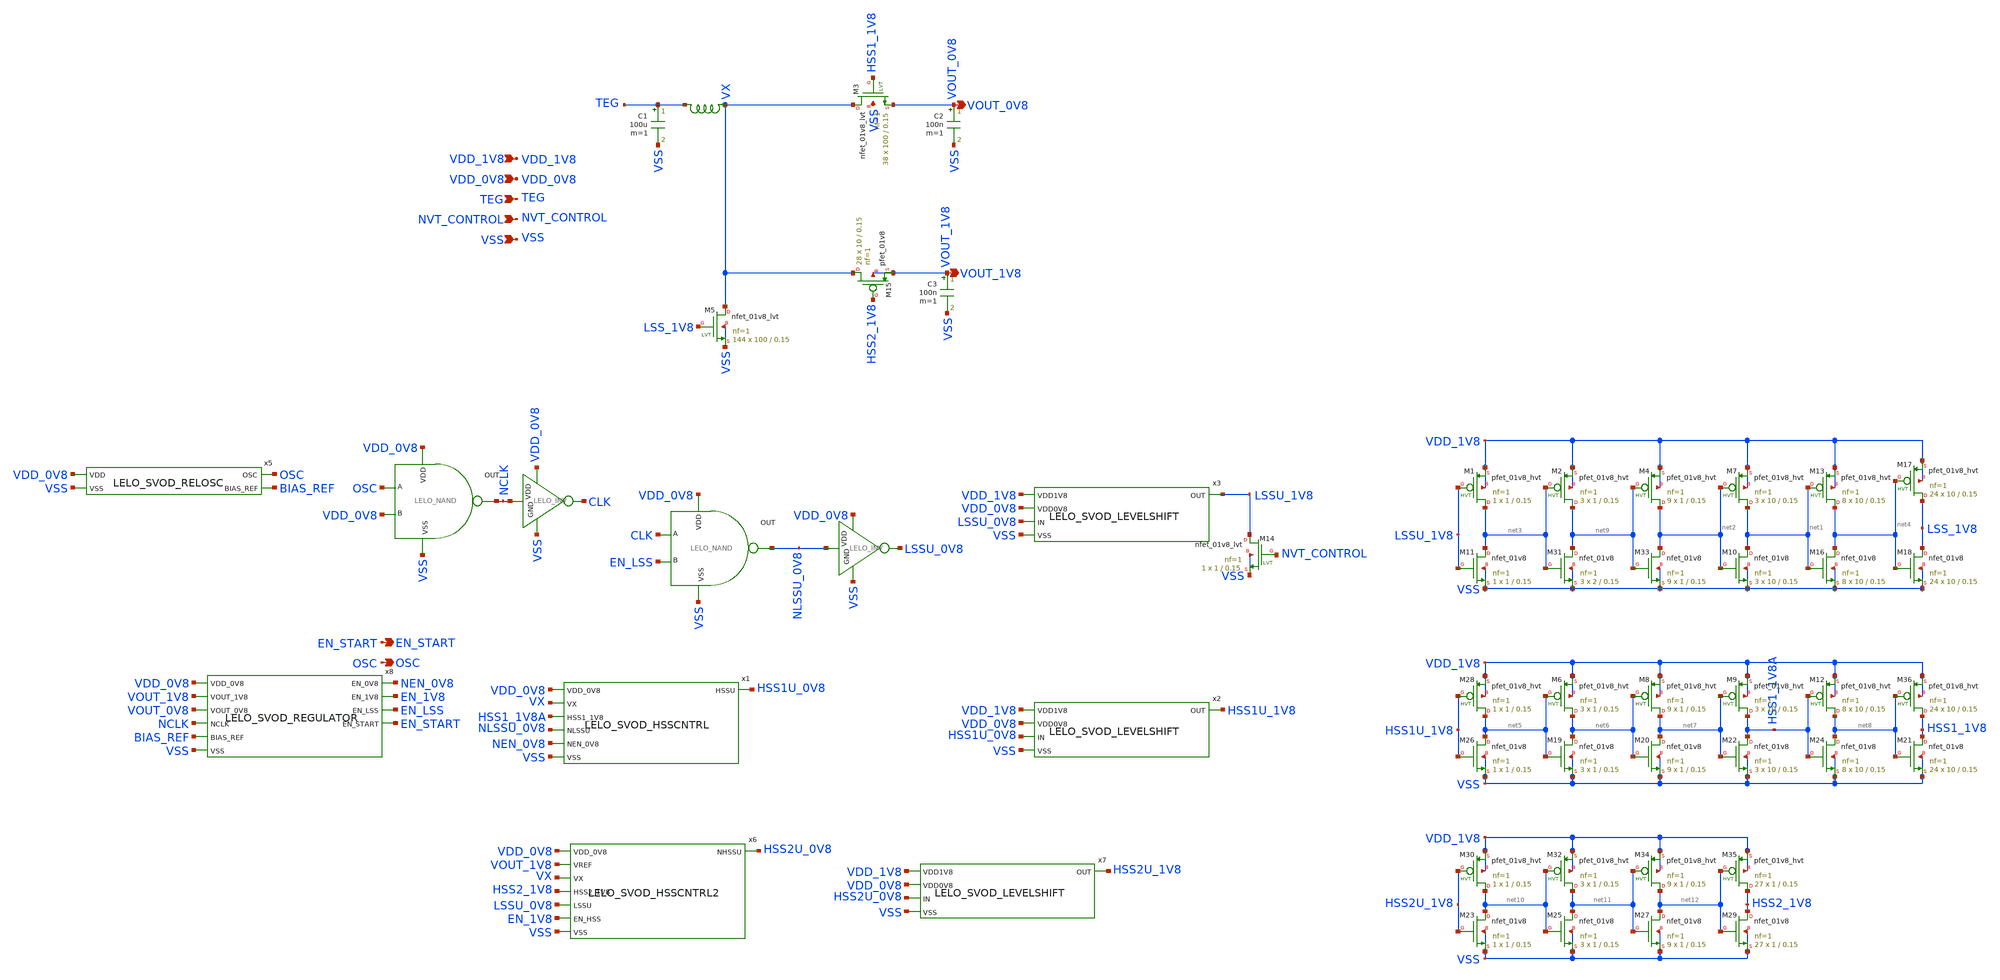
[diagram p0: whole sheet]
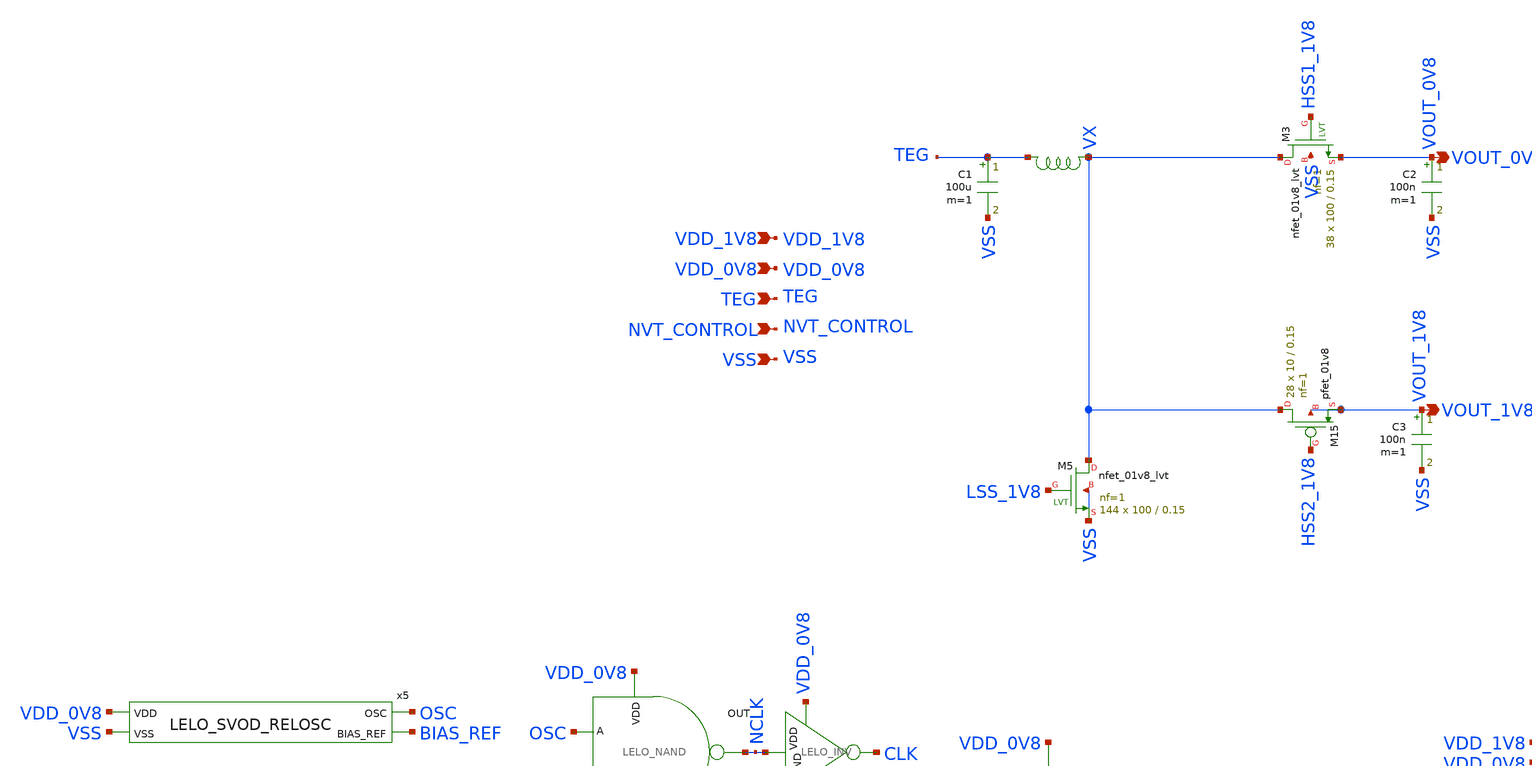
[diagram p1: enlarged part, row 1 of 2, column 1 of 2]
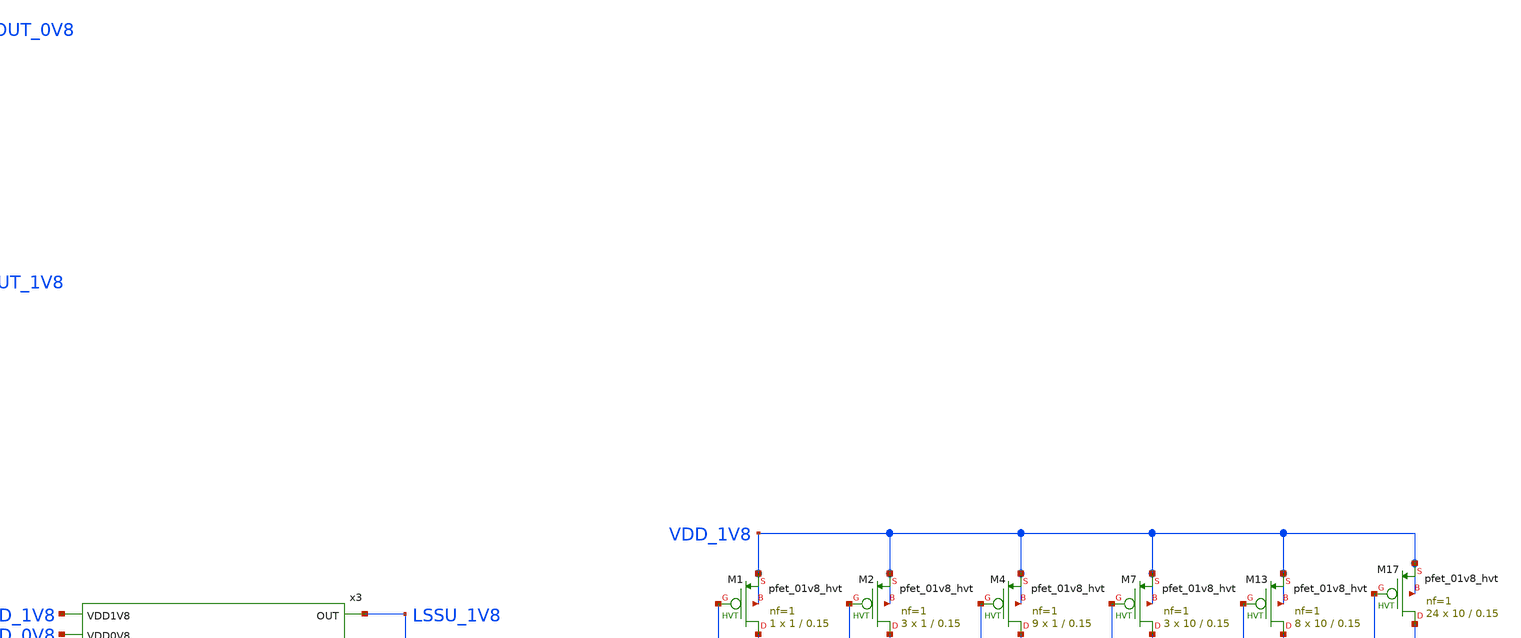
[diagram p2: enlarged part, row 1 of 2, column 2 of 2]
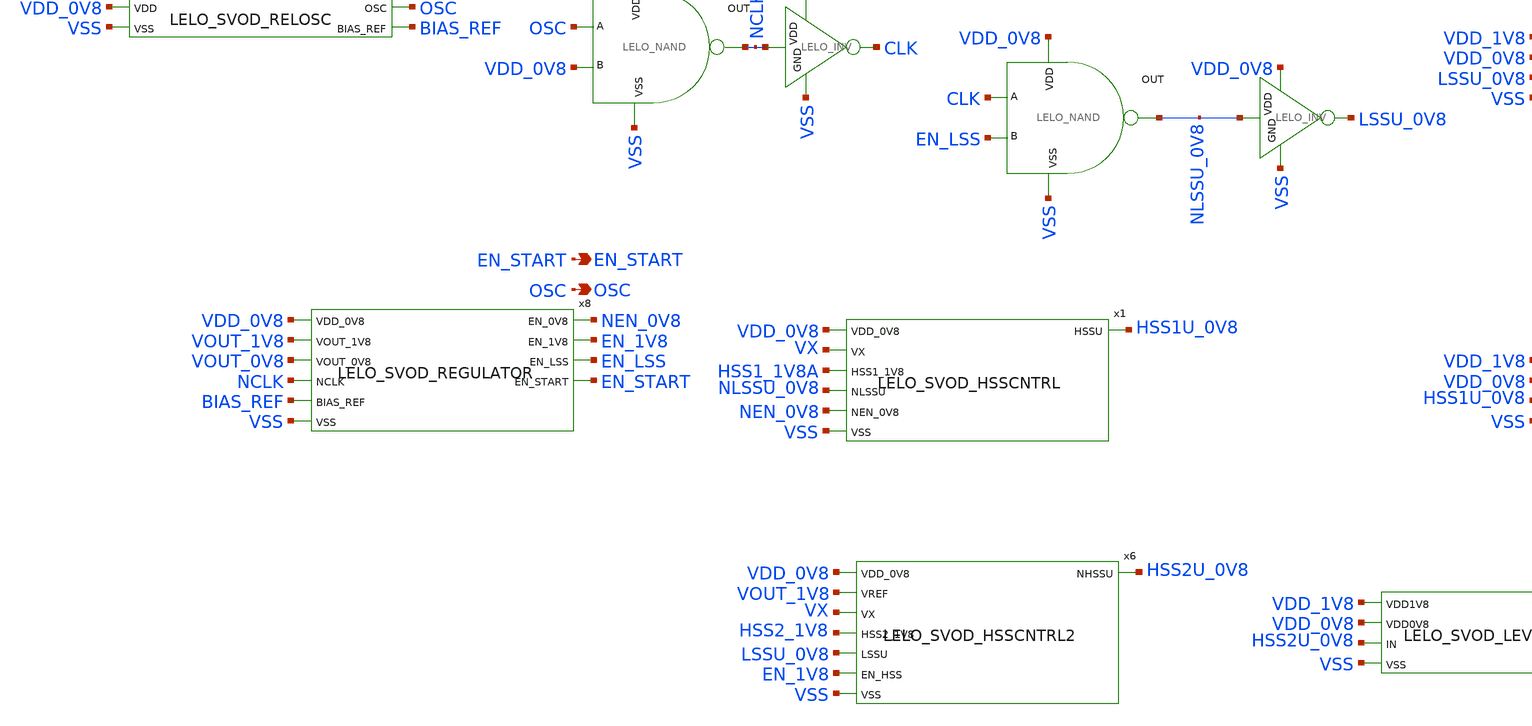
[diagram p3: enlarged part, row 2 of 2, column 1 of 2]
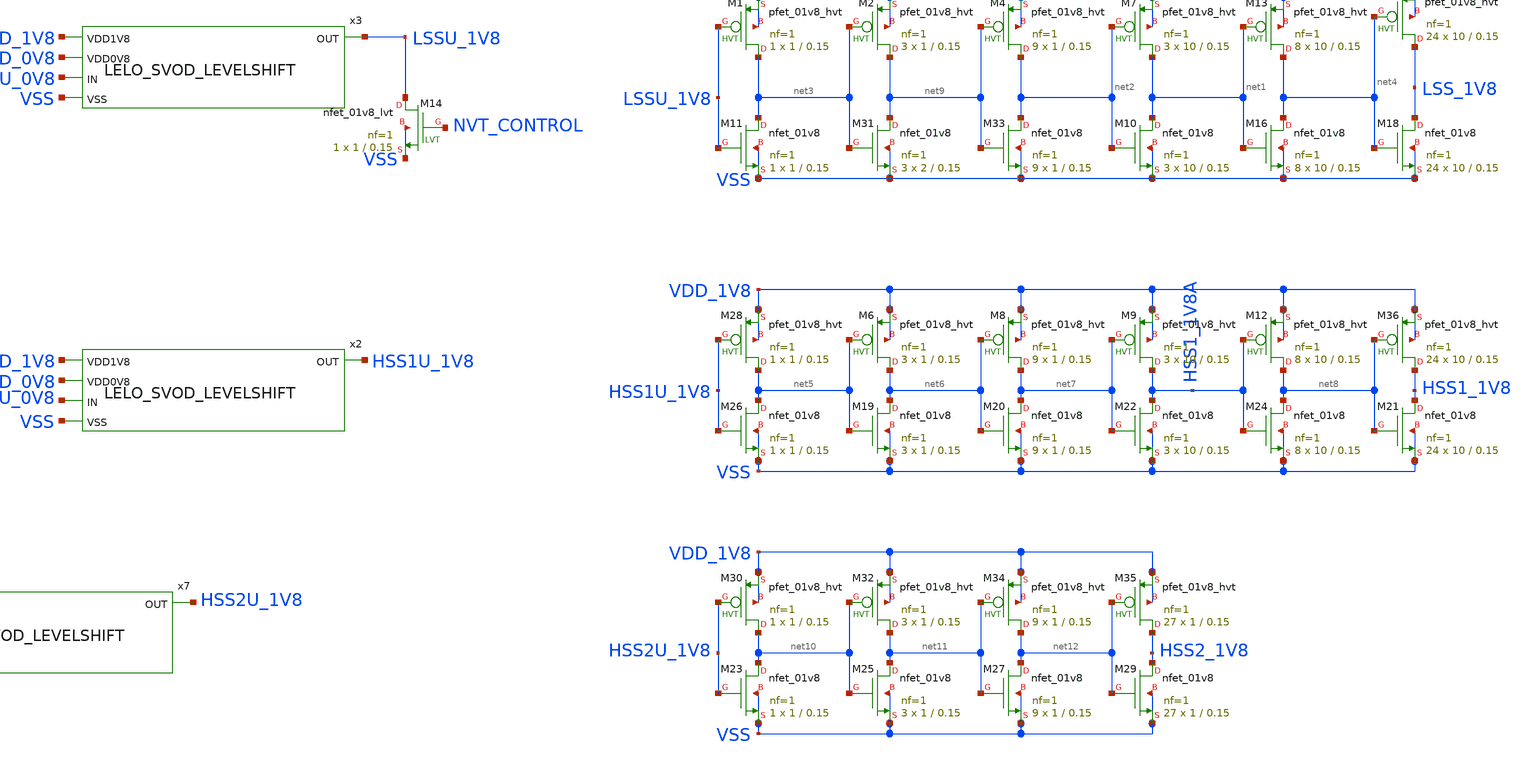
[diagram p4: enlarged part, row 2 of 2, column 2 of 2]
** sch_path: design/LELO_SVOD_SKY130A/LELO_SVOD_BOOST_2.sch
**.subckt LELO_SVOD_BOOST_2 VSS TEG VDD_0V8 VDD_1V8 VOUT_0V8 VOUT_1V8 EN_START OSC NVT_CONTROL
*.ipin VSS
*.ipin TEG
*.ipin VDD_0V8
*.ipin VDD_1V8
*.opin VOUT_0V8
*.opin VOUT_1V8
*.opin EN_START
*.opin OSC
*.ipin NVT_CONTROL
C1 TEG VSS 100u m=1
XM5 VX LSS_1V8 VSS VSS sky130_fd_pr__nfet_01v8_lvt L=0.15 W=100 nf=1 ad='int((1 + 1)/2) * 100 / 1 * 0.29'
+ as='int((1 + 2)/2) * 100 / 1 * 0.29' pd='2*int((1 + 1)/2) * (100 / 1 + 0.29)' ps='2*int((1 + 2)/2) * (100 / 1 + 0.29)'
+ nrd='0.29 / 100 ' nrs='0.29 / 100 ' sa=0 sb=0 sd=0 mult=144 m=144
C2 VOUT_0V8 VSS 100n m=1
XM11 net3 LSSU_1V8 VSS VSS sky130_fd_pr__nfet_01v8 L=0.15 W=1 nf=1 ad='int((1 + 1)/2) * 1 / 1 * 0.29'
+ as='int((1 + 2)/2) * 1 / 1 * 0.29' pd='2*int((1 + 1)/2) * (1 / 1 + 0.29)' ps='2*int((1 + 2)/2) * (1 / 1 + 0.29)'
+ nrd='0.29 / 1 ' nrs='0.29 / 1 ' sa=0 sb=0 sd=0 mult=1 m=1
XM24 net8 HSS1_1V8A VSS VSS sky130_fd_pr__nfet_01v8 L=0.15 W=10 nf=1 ad='int((1 + 1)/2) * 10 / 1 * 0.29'
+ as='int((1 + 2)/2) * 10 / 1 * 0.29' pd='2*int((1 + 1)/2) * (10 / 1 + 0.29)' ps='2*int((1 + 2)/2) * (10 / 1 + 0.29)'
+ nrd='0.29 / 10 ' nrs='0.29 / 10 ' sa=0 sb=0 sd=0 mult=8 m=8
XM31 net9 net3 VSS VSS sky130_fd_pr__nfet_01v8 L=0.15 W=2 nf=1 ad='int((1 + 1)/2) * 2 / 1 * 0.29' as='int((1 + 2)/2) * 2 / 1 * 0.29'
+ pd='2*int((1 + 1)/2) * (2 / 1 + 0.29)' ps='2*int((1 + 2)/2) * (2 / 1 + 0.29)' nrd='0.29 / 2 ' nrs='0.29 / 2 '
+ sa=0 sb=0 sd=0 mult=3 m=3
XM33 net2 net9 VSS VSS sky130_fd_pr__nfet_01v8 L=0.15 W=1 nf=1 ad='int((1 + 1)/2) * 1 / 1 * 0.29' as='int((1 + 2)/2) * 1 / 1 * 0.29'
+ pd='2*int((1 + 1)/2) * (1 / 1 + 0.29)' ps='2*int((1 + 2)/2) * (1 / 1 + 0.29)' nrd='0.29 / 1 ' nrs='0.29 / 1 '
+ sa=0 sb=0 sd=0 mult=9 m=9
XM3 VX HSS1_1V8 VOUT_0V8 VSS sky130_fd_pr__nfet_01v8_lvt L=0.15 W=100 nf=1 ad='int((1 + 1)/2) * 100 / 1 * 0.29'
+ as='int((1 + 2)/2) * 100 / 1 * 0.29' pd='2*int((1 + 1)/2) * (100 / 1 + 0.29)' ps='2*int((1 + 2)/2) * (100 / 1 + 0.29)'
+ nrd='0.29 / 100 ' nrs='0.29 / 100 ' sa=0 sb=0 sd=0 mult=38 m=38
x1 VDD_0V8 VX HSS1_1V8A NLSSU_0V8 HSS1U_0V8 NEN_0V8 VSS LELO_SVOD_HSSCNTRL
x2 VDD_1V8 HSS1U_1V8 VDD_0V8 HSS1U_0V8 VSS LELO_SVOD_LEVELSHIFT
x3 VDD_1V8 LSSU_1V8 VDD_0V8 LSSU_0V8 VSS LELO_SVOD_LEVELSHIFT
XM12 net8 HSS1_1V8A VDD_1V8 VDD_1V8 sky130_fd_pr__pfet_01v8_hvt L=0.15 W=10 nf=1 ad='int((1 + 1)/2) * 10 / 1 * 0.29'
+ as='int((1 + 2)/2) * 10 / 1 * 0.29' pd='2*int((1 + 1)/2) * (10 / 1 + 0.29)' ps='2*int((1 + 2)/2) * (10 / 1 + 0.29)'
+ nrd='0.29 / 10 ' nrs='0.29 / 10 ' sa=0 sb=0 sd=0 mult=8 m=8
XM1 net3 LSSU_1V8 VDD_1V8 VDD_1V8 sky130_fd_pr__pfet_01v8_hvt L=0.15 W=1 nf=1 ad='int((1 + 1)/2) * 1 / 1 * 0.29'
+ as='int((1 + 2)/2) * 1 / 1 * 0.29' pd='2*int((1 + 1)/2) * (1 / 1 + 0.29)' ps='2*int((1 + 2)/2) * (1 / 1 + 0.29)'
+ nrd='0.29 / 1 ' nrs='0.29 / 1 ' sa=0 sb=0 sd=0 mult=1 m=1
XM2 net9 net3 VDD_1V8 VDD_1V8 sky130_fd_pr__pfet_01v8_hvt L=0.15 W=1 nf=1 ad='int((1 + 1)/2) * 1 / 1 * 0.29'
+ as='int((1 + 2)/2) * 1 / 1 * 0.29' pd='2*int((1 + 1)/2) * (1 / 1 + 0.29)' ps='2*int((1 + 2)/2) * (1 / 1 + 0.29)'
+ nrd='0.29 / 1 ' nrs='0.29 / 1 ' sa=0 sb=0 sd=0 mult=3 m=3
XM4 net2 net9 VDD_1V8 VDD_1V8 sky130_fd_pr__pfet_01v8_hvt L=0.15 W=1 nf=1 ad='int((1 + 1)/2) * 1 / 1 * 0.29'
+ as='int((1 + 2)/2) * 1 / 1 * 0.29' pd='2*int((1 + 1)/2) * (1 / 1 + 0.29)' ps='2*int((1 + 2)/2) * (1 / 1 + 0.29)'
+ nrd='0.29 / 1 ' nrs='0.29 / 1 ' sa=0 sb=0 sd=0 mult=9 m=9
x4 VX TEG XGL6030-183_sat
x5 VDD_0V8 OSC BIAS_REF VSS LELO_SVOD_RELOSC
XM15 VX HSS2_1V8 VOUT_1V8 VOUT_1V8 sky130_fd_pr__pfet_01v8 L=0.15 W=10 nf=1 ad='int((1 + 1)/2) * 10 / 1 * 0.29'
+ as='int((1 + 2)/2) * 10 / 1 * 0.29' pd='2*int((1 + 1)/2) * (10 / 1 + 0.29)' ps='2*int((1 + 2)/2) * (10 / 1 + 0.29)'
+ nrd='0.29 / 10 ' nrs='0.29 / 10 ' sa=0 sb=0 sd=0 mult=28 m=28
C3 VOUT_1V8 VSS 100n m=1
x6 VDD_0V8 HSS2U_0V8 VOUT_1V8 VX HSS2_1V8 LSSU_0V8 EN_1V8 VSS LELO_SVOD_HSSCNTRL2
x7 VDD_1V8 HSS2U_1V8 VDD_0V8 HSS2U_0V8 VSS LELO_SVOD_LEVELSHIFT
XM23 net10 HSS2U_1V8 VSS VSS sky130_fd_pr__nfet_01v8 L=0.15 W=1 nf=1 ad='int((1 + 1)/2) * 1 / 1 * 0.29'
+ as='int((1 + 2)/2) * 1 / 1 * 0.29' pd='2*int((1 + 1)/2) * (1 / 1 + 0.29)' ps='2*int((1 + 2)/2) * (1 / 1 + 0.29)'
+ nrd='0.29 / 1 ' nrs='0.29 / 1 ' sa=0 sb=0 sd=0 mult=1 m=1
XM25 net11 net10 VSS VSS sky130_fd_pr__nfet_01v8 L=0.15 W=1 nf=1 ad='int((1 + 1)/2) * 1 / 1 * 0.29' as='int((1 + 2)/2) * 1 / 1 * 0.29'
+ pd='2*int((1 + 1)/2) * (1 / 1 + 0.29)' ps='2*int((1 + 2)/2) * (1 / 1 + 0.29)' nrd='0.29 / 1 ' nrs='0.29 / 1 '
+ sa=0 sb=0 sd=0 mult=3 m=3
XM27 net12 net11 VSS VSS sky130_fd_pr__nfet_01v8 L=0.15 W=1 nf=1 ad='int((1 + 1)/2) * 1 / 1 * 0.29' as='int((1 + 2)/2) * 1 / 1 * 0.29'
+ pd='2*int((1 + 1)/2) * (1 / 1 + 0.29)' ps='2*int((1 + 2)/2) * (1 / 1 + 0.29)' nrd='0.29 / 1 ' nrs='0.29 / 1 '
+ sa=0 sb=0 sd=0 mult=9 m=9
XM29 HSS2_1V8 net12 VSS VSS sky130_fd_pr__nfet_01v8 L=0.15 W=1 nf=1 ad='int((1 + 1)/2) * 1 / 1 * 0.29'
+ as='int((1 + 2)/2) * 1 / 1 * 0.29' pd='2*int((1 + 1)/2) * (1 / 1 + 0.29)' ps='2*int((1 + 2)/2) * (1 / 1 + 0.29)'
+ nrd='0.29 / 1 ' nrs='0.29 / 1 ' sa=0 sb=0 sd=0 mult=27 m=27
XM30 net10 HSS2U_1V8 VDD_1V8 VDD_1V8 sky130_fd_pr__pfet_01v8_hvt L=0.15 W=1 nf=1 ad='int((1 + 1)/2) * 1 / 1 * 0.29'
+ as='int((1 + 2)/2) * 1 / 1 * 0.29' pd='2*int((1 + 1)/2) * (1 / 1 + 0.29)' ps='2*int((1 + 2)/2) * (1 / 1 + 0.29)'
+ nrd='0.29 / 1 ' nrs='0.29 / 1 ' sa=0 sb=0 sd=0 mult=1 m=1
XM32 net11 net10 VDD_1V8 VDD_1V8 sky130_fd_pr__pfet_01v8_hvt L=0.15 W=1 nf=1 ad='int((1 + 1)/2) * 1 / 1 * 0.29'
+ as='int((1 + 2)/2) * 1 / 1 * 0.29' pd='2*int((1 + 1)/2) * (1 / 1 + 0.29)' ps='2*int((1 + 2)/2) * (1 / 1 + 0.29)'
+ nrd='0.29 / 1 ' nrs='0.29 / 1 ' sa=0 sb=0 sd=0 mult=3 m=3
XM34 net12 net11 VDD_1V8 VDD_1V8 sky130_fd_pr__pfet_01v8_hvt L=0.15 W=1 nf=1 ad='int((1 + 1)/2) * 1 / 1 * 0.29'
+ as='int((1 + 2)/2) * 1 / 1 * 0.29' pd='2*int((1 + 1)/2) * (1 / 1 + 0.29)' ps='2*int((1 + 2)/2) * (1 / 1 + 0.29)'
+ nrd='0.29 / 1 ' nrs='0.29 / 1 ' sa=0 sb=0 sd=0 mult=9 m=9
XM35 HSS2_1V8 net12 VDD_1V8 VDD_1V8 sky130_fd_pr__pfet_01v8_hvt L=0.15 W=1 nf=1 ad='int((1 + 1)/2) * 1 / 1 * 0.29'
+ as='int((1 + 2)/2) * 1 / 1 * 0.29' pd='2*int((1 + 1)/2) * (1 / 1 + 0.29)' ps='2*int((1 + 2)/2) * (1 / 1 + 0.29)'
+ nrd='0.29 / 1 ' nrs='0.29 / 1 ' sa=0 sb=0 sd=0 mult=27 m=27
x8 NEN_0V8 EN_1V8 EN_LSS VDD_0V8 EN_START VOUT_1V8 VOUT_0V8 NCLK BIAS_REF VSS LELO_SVOD_REGULATOR
x9 VDD_0V8 NLSSU_0V8 CLK EN_LSS VSS LELO_NAND
x10 VDD_0V8 NLSSU_0V8 LSSU_0V8 VSS LELO_INV
x11 VDD_0V8 NCLK CLK VSS LELO_INV
x13 VDD_0V8 NCLK OSC VDD_0V8 VSS LELO_NAND
XM14 LSSU_1V8 NVT_CONTROL VSS VSS sky130_fd_pr__nfet_01v8_lvt L=0.15 W=1 nf=1 ad='int((1 + 1)/2) * 1 / 1 * 0.29'
+ as='int((1 + 2)/2) * 1 / 1 * 0.29' pd='2*int((1 + 1)/2) * (1 / 1 + 0.29)' ps='2*int((1 + 2)/2) * (1 / 1 + 0.29)'
+ nrd='0.29 / 1 ' nrs='0.29 / 1 ' sa=0 sb=0 sd=0 mult=1 m=1
XM26 net5 HSS1U_1V8 VSS VSS sky130_fd_pr__nfet_01v8 L=0.15 W=1 nf=1 ad='int((1 + 1)/2) * 1 / 1 * 0.29'
+ as='int((1 + 2)/2) * 1 / 1 * 0.29' pd='2*int((1 + 1)/2) * (1 / 1 + 0.29)' ps='2*int((1 + 2)/2) * (1 / 1 + 0.29)'
+ nrd='0.29 / 1 ' nrs='0.29 / 1 ' sa=0 sb=0 sd=0 mult=1 m=1
XM28 net5 HSS1U_1V8 VDD_1V8 VDD_1V8 sky130_fd_pr__pfet_01v8_hvt L=0.15 W=1 nf=1 ad='int((1 + 1)/2) * 1 / 1 * 0.29'
+ as='int((1 + 2)/2) * 1 / 1 * 0.29' pd='2*int((1 + 1)/2) * (1 / 1 + 0.29)' ps='2*int((1 + 2)/2) * (1 / 1 + 0.29)'
+ nrd='0.29 / 1 ' nrs='0.29 / 1 ' sa=0 sb=0 sd=0 mult=1 m=1
XM21 HSS1_1V8 net8 VSS VSS sky130_fd_pr__nfet_01v8 L=0.15 W=10 nf=1 ad='int((1 + 1)/2) * 10 / 1 * 0.29'
+ as='int((1 + 2)/2) * 10 / 1 * 0.29' pd='2*int((1 + 1)/2) * (10 / 1 + 0.29)' ps='2*int((1 + 2)/2) * (10 / 1 + 0.29)'
+ nrd='0.29 / 10 ' nrs='0.29 / 10 ' sa=0 sb=0 sd=0 mult=24 m=24
XM36 HSS1_1V8 net8 VDD_1V8 VDD_1V8 sky130_fd_pr__pfet_01v8_hvt L=0.15 W=10 nf=1 ad='int((1 + 1)/2) * 10 / 1 * 0.29'
+ as='int((1 + 2)/2) * 10 / 1 * 0.29' pd='2*int((1 + 1)/2) * (10 / 1 + 0.29)' ps='2*int((1 + 2)/2) * (10 / 1 + 0.29)'
+ nrd='0.29 / 10 ' nrs='0.29 / 10 ' sa=0 sb=0 sd=0 mult=24 m=24
XM6 net6 net5 VDD_1V8 VDD_1V8 sky130_fd_pr__pfet_01v8_hvt L=0.15 W=1 nf=1 ad='int((1 + 1)/2) * 1 / 1 * 0.29'
+ as='int((1 + 2)/2) * 1 / 1 * 0.29' pd='2*int((1 + 1)/2) * (1 / 1 + 0.29)' ps='2*int((1 + 2)/2) * (1 / 1 + 0.29)'
+ nrd='0.29 / 1 ' nrs='0.29 / 1 ' sa=0 sb=0 sd=0 mult=3 m=3
XM19 net6 net5 VSS VSS sky130_fd_pr__nfet_01v8 L=0.15 W=1 nf=1 ad='int((1 + 1)/2) * 1 / 1 * 0.29' as='int((1 + 2)/2) * 1 / 1 * 0.29'
+ pd='2*int((1 + 1)/2) * (1 / 1 + 0.29)' ps='2*int((1 + 2)/2) * (1 / 1 + 0.29)' nrd='0.29 / 1 ' nrs='0.29 / 1 '
+ sa=0 sb=0 sd=0 mult=3 m=3
XM8 net7 net6 VDD_1V8 VDD_1V8 sky130_fd_pr__pfet_01v8_hvt L=0.15 W=1 nf=1 ad='int((1 + 1)/2) * 1 / 1 * 0.29'
+ as='int((1 + 2)/2) * 1 / 1 * 0.29' pd='2*int((1 + 1)/2) * (1 / 1 + 0.29)' ps='2*int((1 + 2)/2) * (1 / 1 + 0.29)'
+ nrd='0.29 / 1 ' nrs='0.29 / 1 ' sa=0 sb=0 sd=0 mult=9 m=9
XM20 net7 net6 VSS VSS sky130_fd_pr__nfet_01v8 L=0.15 W=1 nf=1 ad='int((1 + 1)/2) * 1 / 1 * 0.29' as='int((1 + 2)/2) * 1 / 1 * 0.29'
+ pd='2*int((1 + 1)/2) * (1 / 1 + 0.29)' ps='2*int((1 + 2)/2) * (1 / 1 + 0.29)' nrd='0.29 / 1 ' nrs='0.29 / 1 '
+ sa=0 sb=0 sd=0 mult=9 m=9
XM9 HSS1_1V8A net7 VDD_1V8 VDD_1V8 sky130_fd_pr__pfet_01v8_hvt L=0.15 W=10 nf=1 ad='int((1 + 1)/2) * 10 / 1 * 0.29'
+ as='int((1 + 2)/2) * 10 / 1 * 0.29' pd='2*int((1 + 1)/2) * (10 / 1 + 0.29)' ps='2*int((1 + 2)/2) * (10 / 1 + 0.29)'
+ nrd='0.29 / 10 ' nrs='0.29 / 10 ' sa=0 sb=0 sd=0 mult=3 m=3
XM22 HSS1_1V8A net7 VSS VSS sky130_fd_pr__nfet_01v8 L=0.15 W=10 nf=1 ad='int((1 + 1)/2) * 10 / 1 * 0.29'
+ as='int((1 + 2)/2) * 10 / 1 * 0.29' pd='2*int((1 + 1)/2) * (10 / 1 + 0.29)' ps='2*int((1 + 2)/2) * (10 / 1 + 0.29)'
+ nrd='0.29 / 10 ' nrs='0.29 / 10 ' sa=0 sb=0 sd=0 mult=3 m=3
XM7 net1 net2 VDD_1V8 VDD_1V8 sky130_fd_pr__pfet_01v8_hvt L=0.15 W=10 nf=1 ad='int((1 + 1)/2) * 10 / 1 * 0.29'
+ as='int((1 + 2)/2) * 10 / 1 * 0.29' pd='2*int((1 + 1)/2) * (10 / 1 + 0.29)' ps='2*int((1 + 2)/2) * (10 / 1 + 0.29)'
+ nrd='0.29 / 10 ' nrs='0.29 / 10 ' sa=0 sb=0 sd=0 mult=3 m=3
XM10 net1 net2 VSS VSS sky130_fd_pr__nfet_01v8 L=0.15 W=10 nf=1 ad='int((1 + 1)/2) * 10 / 1 * 0.29' as='int((1 + 2)/2) * 10 / 1 * 0.29'
+ pd='2*int((1 + 1)/2) * (10 / 1 + 0.29)' ps='2*int((1 + 2)/2) * (10 / 1 + 0.29)' nrd='0.29 / 10 ' nrs='0.29 / 10 '
+ sa=0 sb=0 sd=0 mult=3 m=3
XM13 net4 net1 VDD_1V8 VDD_1V8 sky130_fd_pr__pfet_01v8_hvt L=0.15 W=10 nf=1 ad='int((1 + 1)/2) * 10 / 1 * 0.29'
+ as='int((1 + 2)/2) * 10 / 1 * 0.29' pd='2*int((1 + 1)/2) * (10 / 1 + 0.29)' ps='2*int((1 + 2)/2) * (10 / 1 + 0.29)'
+ nrd='0.29 / 10 ' nrs='0.29 / 10 ' sa=0 sb=0 sd=0 mult=8 m=8
XM16 net4 net1 VSS VSS sky130_fd_pr__nfet_01v8 L=0.15 W=10 nf=1 ad='int((1 + 1)/2) * 10 / 1 * 0.29' as='int((1 + 2)/2) * 10 / 1 * 0.29'
+ pd='2*int((1 + 1)/2) * (10 / 1 + 0.29)' ps='2*int((1 + 2)/2) * (10 / 1 + 0.29)' nrd='0.29 / 10 ' nrs='0.29 / 10 '
+ sa=0 sb=0 sd=0 mult=8 m=8
XM17 LSS_1V8 net4 VDD_1V8 VDD_1V8 sky130_fd_pr__pfet_01v8_hvt L=0.15 W=10 nf=1 ad='int((1 + 1)/2) * 10 / 1 * 0.29'
+ as='int((1 + 2)/2) * 10 / 1 * 0.29' pd='2*int((1 + 1)/2) * (10 / 1 + 0.29)' ps='2*int((1 + 2)/2) * (10 / 1 + 0.29)'
+ nrd='0.29 / 10 ' nrs='0.29 / 10 ' sa=0 sb=0 sd=0 mult=24 m=24
XM18 LSS_1V8 net4 VSS VSS sky130_fd_pr__nfet_01v8 L=0.15 W=10 nf=1 ad='int((1 + 1)/2) * 10 / 1 * 0.29'
+ as='int((1 + 2)/2) * 10 / 1 * 0.29' pd='2*int((1 + 1)/2) * (10 / 1 + 0.29)' ps='2*int((1 + 2)/2) * (10 / 1 + 0.29)'
+ nrd='0.29 / 10 ' nrs='0.29 / 10 ' sa=0 sb=0 sd=0 mult=24 m=24
**.ends
.end
